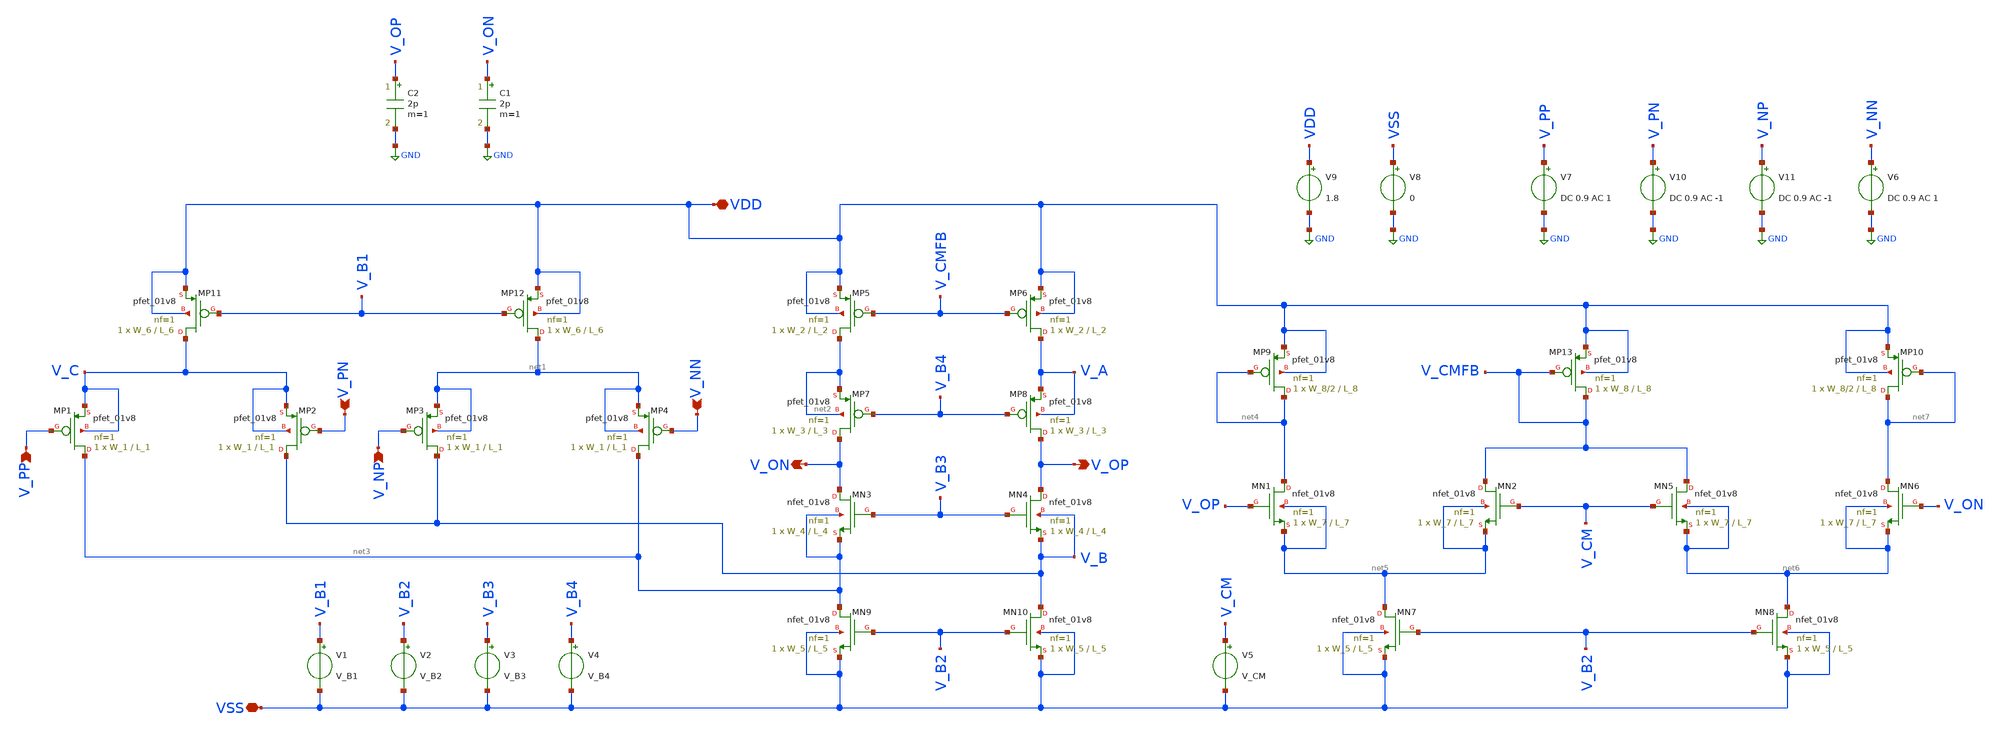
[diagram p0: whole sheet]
** sch_path: Xschem Simulations/FDDA_CMFB/tb_FDDA_CMFB_ac_dm.sch
**.subckt tb_FDDA_CMFB_ac_dm V_PP V_PN V_NP V_NN VDD VSS V_OP V_ON
*.ipin V_PP
*.ipin V_PN
*.ipin V_NP
*.ipin V_NN
*.iopin VDD
*.iopin VSS
*.opin V_OP
*.opin V_ON
XMP1 net3 V_PP V_C V_C sky130_fd_pr__pfet_01v8 L=L_1 W=W_1 nf=1 ad='int((1 + 1)/2) * W_1 / 1 * 0.29'
+ as='int((1 + 2)/2) * W_1 / 1 * 0.29' pd='2*int((1 + 1)/2) * (W_1 / 1 + 0.29)' ps='2*int((1 + 2)/2) * (W_1 / 1 + 0.29)'
+ nrd='0.29 / W_1 ' nrs='0.29 / W_1 ' sa=0 sb=0 sd=0 mult=1 m=1
XMP2 V_B V_PN V_C V_C sky130_fd_pr__pfet_01v8 L=L_1 W=W_1 nf=1 ad='int((1 + 1)/2) * W_1 / 1 * 0.29' as='int((1 + 2)/2) * W_1 / 1 * 0.29'
+ pd='2*int((1 + 1)/2) * (W_1 / 1 + 0.29)' ps='2*int((1 + 2)/2) * (W_1 / 1 + 0.29)' nrd='0.29 / W_1 ' nrs='0.29 / W_1 '
+ sa=0 sb=0 sd=0 mult=1 m=1
XMP3 V_B V_NP net1 net1 sky130_fd_pr__pfet_01v8 L=L_1 W=W_1 nf=1 ad='int((1 + 1)/2) * W_1 / 1 * 0.29'
+ as='int((1 + 2)/2) * W_1 / 1 * 0.29' pd='2*int((1 + 1)/2) * (W_1 / 1 + 0.29)' ps='2*int((1 + 2)/2) * (W_1 / 1 + 0.29)'
+ nrd='0.29 / W_1 ' nrs='0.29 / W_1 ' sa=0 sb=0 sd=0 mult=1 m=1
XMP4 net3 V_NN net1 net1 sky130_fd_pr__pfet_01v8 L=L_1 W=W_1 nf=1 ad='int((1 + 1)/2) * W_1 / 1 * 0.29'
+ as='int((1 + 2)/2) * W_1 / 1 * 0.29' pd='2*int((1 + 1)/2) * (W_1 / 1 + 0.29)' ps='2*int((1 + 2)/2) * (W_1 / 1 + 0.29)'
+ nrd='0.29 / W_1 ' nrs='0.29 / W_1 ' sa=0 sb=0 sd=0 mult=1 m=1
XMP5 net2 V_CMFB VDD VDD sky130_fd_pr__pfet_01v8 L=L_2 W=W_2 nf=1 ad='int((1 + 1)/2) * W_2 / 1 * 0.29'
+ as='int((1 + 2)/2) * W_2 / 1 * 0.29' pd='2*int((1 + 1)/2) * (W_2 / 1 + 0.29)' ps='2*int((1 + 2)/2) * (W_2 / 1 + 0.29)'
+ nrd='0.29 / W_2 ' nrs='0.29 / W_2 ' sa=0 sb=0 sd=0 mult=1 m=1
XMP6 V_A V_CMFB VDD VDD sky130_fd_pr__pfet_01v8 L=L_2 W=W_2 nf=1 ad='int((1 + 1)/2) * W_2 / 1 * 0.29'
+ as='int((1 + 2)/2) * W_2 / 1 * 0.29' pd='2*int((1 + 1)/2) * (W_2 / 1 + 0.29)' ps='2*int((1 + 2)/2) * (W_2 / 1 + 0.29)'
+ nrd='0.29 / W_2 ' nrs='0.29 / W_2 ' sa=0 sb=0 sd=0 mult=1 m=1
XMP7 V_ON V_B4 net2 net2 sky130_fd_pr__pfet_01v8 L=L_3 W=W_3 nf=1 ad='int((1 + 1)/2) * W_3 / 1 * 0.29'
+ as='int((1 + 2)/2) * W_3 / 1 * 0.29' pd='2*int((1 + 1)/2) * (W_3 / 1 + 0.29)' ps='2*int((1 + 2)/2) * (W_3 / 1 + 0.29)'
+ nrd='0.29 / W_3 ' nrs='0.29 / W_3 ' sa=0 sb=0 sd=0 mult=1 m=1
XMP8 V_OP V_B4 V_A V_A sky130_fd_pr__pfet_01v8 L=L_3 W=W_3 nf=1 ad='int((1 + 1)/2) * W_3 / 1 * 0.29'
+ as='int((1 + 2)/2) * W_3 / 1 * 0.29' pd='2*int((1 + 1)/2) * (W_3 / 1 + 0.29)' ps='2*int((1 + 2)/2) * (W_3 / 1 + 0.29)'
+ nrd='0.29 / W_3 ' nrs='0.29 / W_3 ' sa=0 sb=0 sd=0 mult=1 m=1
XMP11 V_C V_B1 VDD VDD sky130_fd_pr__pfet_01v8 L=L_6 W=W_6 nf=1 ad='int((1 + 1)/2) * W_6 / 1 * 0.29'
+ as='int((1 + 2)/2) * W_6 / 1 * 0.29' pd='2*int((1 + 1)/2) * (W_6 / 1 + 0.29)' ps='2*int((1 + 2)/2) * (W_6 / 1 + 0.29)'
+ nrd='0.29 / W_6 ' nrs='0.29 / W_6 ' sa=0 sb=0 sd=0 mult=1 m=1
XMP12 net1 V_B1 VDD VDD sky130_fd_pr__pfet_01v8 L=L_6 W=W_6 nf=1 ad='int((1 + 1)/2) * W_6 / 1 * 0.29'
+ as='int((1 + 2)/2) * W_6 / 1 * 0.29' pd='2*int((1 + 1)/2) * (W_6 / 1 + 0.29)' ps='2*int((1 + 2)/2) * (W_6 / 1 + 0.29)'
+ nrd='0.29 / W_6 ' nrs='0.29 / W_6 ' sa=0 sb=0 sd=0 mult=1 m=1
XMN3 V_ON V_B3 net3 net3 sky130_fd_pr__nfet_01v8 L=L_4 W=W_4 nf=1 ad='int((1 + 1)/2) * W_4 / 1 * 0.29'
+ as='int((1 + 2)/2) * W_4 / 1 * 0.29' pd='2*int((1 + 1)/2) * (W_4 / 1 + 0.29)' ps='2*int((1 + 2)/2) * (W_4 / 1 + 0.29)'
+ nrd='0.29 / W_4 ' nrs='0.29 / W_4 ' sa=0 sb=0 sd=0 mult=1 m=1
XMN4 V_OP V_B3 V_B V_B sky130_fd_pr__nfet_01v8 L=L_4 W=W_4 nf=1 ad='int((1 + 1)/2) * W_4 / 1 * 0.29'
+ as='int((1 + 2)/2) * W_4 / 1 * 0.29' pd='2*int((1 + 1)/2) * (W_4 / 1 + 0.29)' ps='2*int((1 + 2)/2) * (W_4 / 1 + 0.29)'
+ nrd='0.29 / W_4 ' nrs='0.29 / W_4 ' sa=0 sb=0 sd=0 mult=1 m=1
XMN9 net3 V_B2 VSS VSS sky130_fd_pr__nfet_01v8 L=L_5 W=W_5 nf=1 ad='int((1 + 1)/2) * W_5 / 1 * 0.29'
+ as='int((1 + 2)/2) * W_5 / 1 * 0.29' pd='2*int((1 + 1)/2) * (W_5 / 1 + 0.29)' ps='2*int((1 + 2)/2) * (W_5 / 1 + 0.29)'
+ nrd='0.29 / W_5 ' nrs='0.29 / W_5 ' sa=0 sb=0 sd=0 mult=1 m=1
XMN10 V_B V_B2 VSS VSS sky130_fd_pr__nfet_01v8 L=L_5 W=W_5 nf=1 ad='int((1 + 1)/2) * W_5 / 1 * 0.29'
+ as='int((1 + 2)/2) * W_5 / 1 * 0.29' pd='2*int((1 + 1)/2) * (W_5 / 1 + 0.29)' ps='2*int((1 + 2)/2) * (W_5 / 1 + 0.29)'
+ nrd='0.29 / W_5 ' nrs='0.29 / W_5 ' sa=0 sb=0 sd=0 mult=1 m=1
V4 V_B4 VSS V_B4
V3 V_B3 VSS V_B3
V2 V_B2 VSS V_B2
V1 V_B1 VSS V_B1
XMN1 net4 V_OP net5 net5 sky130_fd_pr__nfet_01v8 L=L_7 W=W_7 nf=1 ad='int((1 + 1)/2) * W_7 / 1 * 0.29'
+ as='int((1 + 2)/2) * W_7 / 1 * 0.29' pd='2*int((1 + 1)/2) * (W_7 / 1 + 0.29)' ps='2*int((1 + 2)/2) * (W_7 / 1 + 0.29)'
+ nrd='0.29 / W_7 ' nrs='0.29 / W_7 ' sa=0 sb=0 sd=0 mult=1 m=1
XMN2 V_CMFB V_CM net5 net5 sky130_fd_pr__nfet_01v8 L=L_7 W=W_7 nf=1 ad='int((1 + 1)/2) * W_7 / 1 * 0.29'
+ as='int((1 + 2)/2) * W_7 / 1 * 0.29' pd='2*int((1 + 1)/2) * (W_7 / 1 + 0.29)' ps='2*int((1 + 2)/2) * (W_7 / 1 + 0.29)'
+ nrd='0.29 / W_7 ' nrs='0.29 / W_7 ' sa=0 sb=0 sd=0 mult=1 m=1
XMN7 net5 V_B2 VSS VSS sky130_fd_pr__nfet_01v8 L=L_5 W=W_5 nf=1 ad='int((1 + 1)/2) * W_5 / 1 * 0.29'
+ as='int((1 + 2)/2) * W_5 / 1 * 0.29' pd='2*int((1 + 1)/2) * (W_5 / 1 + 0.29)' ps='2*int((1 + 2)/2) * (W_5 / 1 + 0.29)'
+ nrd='0.29 / W_5 ' nrs='0.29 / W_5 ' sa=0 sb=0 sd=0 mult=1 m=1
XMN6 net7 V_ON net6 net6 sky130_fd_pr__nfet_01v8 L=L_7 W=W_7 nf=1 ad='int((1 + 1)/2) * W_7 / 1 * 0.29'
+ as='int((1 + 2)/2) * W_7 / 1 * 0.29' pd='2*int((1 + 1)/2) * (W_7 / 1 + 0.29)' ps='2*int((1 + 2)/2) * (W_7 / 1 + 0.29)'
+ nrd='0.29 / W_7 ' nrs='0.29 / W_7 ' sa=0 sb=0 sd=0 mult=1 m=1
XMN5 V_CMFB V_CM net6 net6 sky130_fd_pr__nfet_01v8 L=L_7 W=W_7 nf=1 ad='int((1 + 1)/2) * W_7 / 1 * 0.29'
+ as='int((1 + 2)/2) * W_7 / 1 * 0.29' pd='2*int((1 + 1)/2) * (W_7 / 1 + 0.29)' ps='2*int((1 + 2)/2) * (W_7 / 1 + 0.29)'
+ nrd='0.29 / W_7 ' nrs='0.29 / W_7 ' sa=0 sb=0 sd=0 mult=1 m=1
XMN8 net6 V_B2 VSS VSS sky130_fd_pr__nfet_01v8 L=L_5 W=W_5 nf=1 ad='int((1 + 1)/2) * W_5 / 1 * 0.29'
+ as='int((1 + 2)/2) * W_5 / 1 * 0.29' pd='2*int((1 + 1)/2) * (W_5 / 1 + 0.29)' ps='2*int((1 + 2)/2) * (W_5 / 1 + 0.29)'
+ nrd='0.29 / W_5 ' nrs='0.29 / W_5 ' sa=0 sb=0 sd=0 mult=1 m=1
XMP9 net4 net4 VDD VDD sky130_fd_pr__pfet_01v8 L=L_8 W=W_8/2 nf=1 ad='int((1 + 1)/2) * W_8/2 / 1 * 0.29'
+ as='int((1 + 2)/2) * W_8/2 / 1 * 0.29' pd='2*int((1 + 1)/2) * (W_8/2 / 1 + 0.29)' ps='2*int((1 + 2)/2) * (W_8/2 / 1 + 0.29)'
+ nrd='0.29 / W_8/2 ' nrs='0.29 / W_8/2 ' sa=0 sb=0 sd=0 mult=1 m=1
XMP13 V_CMFB V_CMFB VDD VDD sky130_fd_pr__pfet_01v8 L=L_8 W=W_8 nf=1 ad='int((1 + 1)/2) * W_8 / 1 * 0.29'
+ as='int((1 + 2)/2) * W_8 / 1 * 0.29' pd='2*int((1 + 1)/2) * (W_8 / 1 + 0.29)' ps='2*int((1 + 2)/2) * (W_8 / 1 + 0.29)'
+ nrd='0.29 / W_8 ' nrs='0.29 / W_8 ' sa=0 sb=0 sd=0 mult=1 m=1
XMP10 net7 net7 VDD VDD sky130_fd_pr__pfet_01v8 L=L_8 W=W_8/2 nf=1 ad='int((1 + 1)/2) * W_8/2 / 1 * 0.29'
+ as='int((1 + 2)/2) * W_8/2 / 1 * 0.29' pd='2*int((1 + 1)/2) * (W_8/2 / 1 + 0.29)' ps='2*int((1 + 2)/2) * (W_8/2 / 1 + 0.29)'
+ nrd='0.29 / W_8/2 ' nrs='0.29 / W_8/2 ' sa=0 sb=0 sd=0 mult=1 m=1
V5 V_CM VSS V_CM
V10 V_PN GND DC 0.9 AC -1
V7 V_PP GND DC 0.9 AC 1
V8 VSS GND 0
V9 VDD GND 1.8
V6 V_NN GND DC 0.9 AC 1
V11 V_NP GND DC 0.9 AC -1
C1 V_ON GND 2p m=1
C2 V_OP GND 2p m=1
**** begin user architecture code

** opencircuitdesign pdks install
.lib $::SKYWATER_MODELS/sky130.lib.spice tt



.control
  save all
  ac dec 20 0.1 0.1G

  let vout = v(v_op) - v(v_on)
  let vin_dm = (v(v_pp) - v(v_pn)) - (v(v_np) - v(v_nn))

  let gain_dm = vout / vin_dm
  let db_gain_dm = db(gain_dm)
  let deg_phase = 180*cph(v(vout))/pi

  meas ac gain_dm_DC FIND db_gain_dm AT=1

  meas ac gbw_freq WHEN db_gain_dm=0 FALL=1
  let gbw_Mfreq = gbw_freq * 1e-6

  meas ac pm_deg FIND deg_phase AT=gbw_freq
  let pm = 180 + pm_deg

  plot db_gain_dm deg_phase
  print gain_dm_DC
  print gbw_Mfreq
  print pm
  wrdata DM.txt db_gain_dm
.endc




.param temp=25
.option savecurrents
.param W_1=88
.param W_2=88
.param W_3=88
.param W_4=14
.param W_5=28
.param W_6=176
.param W_7=14
.param W_8=176
.param L_1=1
.param L_2=1
.param L_3=1
.param L_4=1
.param L_5=1
.param L_6=1
.param L_7=1
.param L_8=1
.param V_B1=0.7454
.param V_B2=0.6351
.param V_B3=0.8571
.param V_B4=0.5706
.param V_CM=0.9
.control
  save all
  op
  write tb_FDDA_CMFB_ac_dm.raw
.endc


**** end user architecture code
**.ends
.GLOBAL GND
.end
